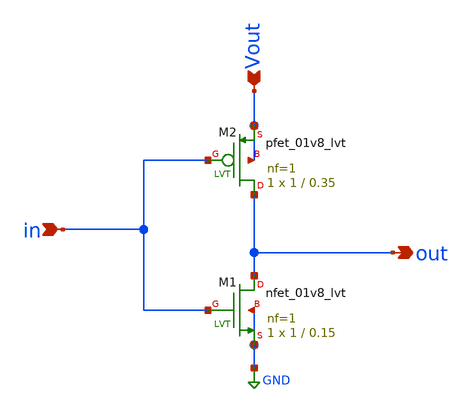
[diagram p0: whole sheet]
** sch_path: Current Sensor/inverter.sch
**.subckt inverter out in Vout
*.opin out
*.ipin in
*.ipin Vout
XM1 out in GND GND sky130_fd_pr__nfet_01v8_lvt L=0.15 W=1 nf=1 ad='int((nf+1)/2) * W/nf * 0.29' as='int((nf+2)/2) * W/nf * 0.29'
+ pd='2*int((nf+1)/2) * (W/nf + 0.29)' ps='2*int((nf+2)/2) * (W/nf + 0.29)' nrd='0.29 / W' nrs='0.29 / W'
+ sa=0 sb=0 sd=0 mult=1 m=1
XM2 out in Vout Vout sky130_fd_pr__pfet_01v8_lvt L=0.35 W=1 nf=1 ad='int((nf+1)/2) * W/nf * 0.29' as='int((nf+2)/2) * W/nf * 0.29'
+ pd='2*int((nf+1)/2) * (W/nf + 0.29)' ps='2*int((nf+2)/2) * (W/nf + 0.29)' nrd='0.29 / W' nrs='0.29 / W'
+ sa=0 sb=0 sd=0 mult=1 m=1
**.ends
.GLOBAL GND
.end
